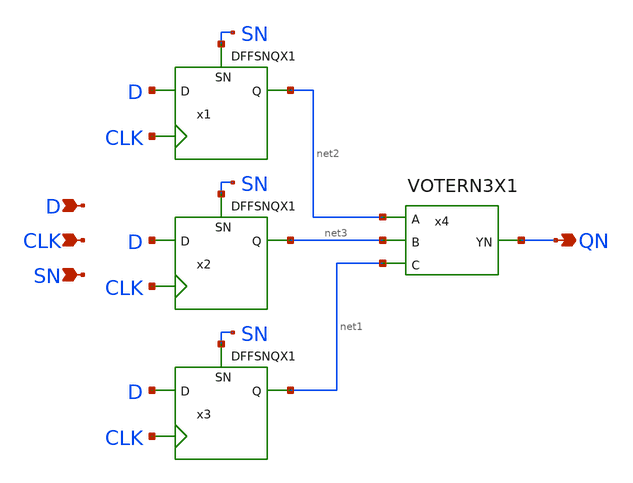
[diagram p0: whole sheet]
** sch_path: current/xschem/TMRDFFSNQNX1.sch
**.subckt TMRDFFSNQNX1 QN D CLK SN
*.opin QN
*.ipin D
*.ipin CLK
*.ipin SN
x4 net2 net3 net1 QN VDD VSS VOTERN3X1
x1 net2 D CLK SN VDD VSS DFFSNQX1
x2 net3 D CLK SN VDD VSS DFFSNQX1
x3 net1 D CLK SN VDD VSS DFFSNQX1
**.ends
.end
